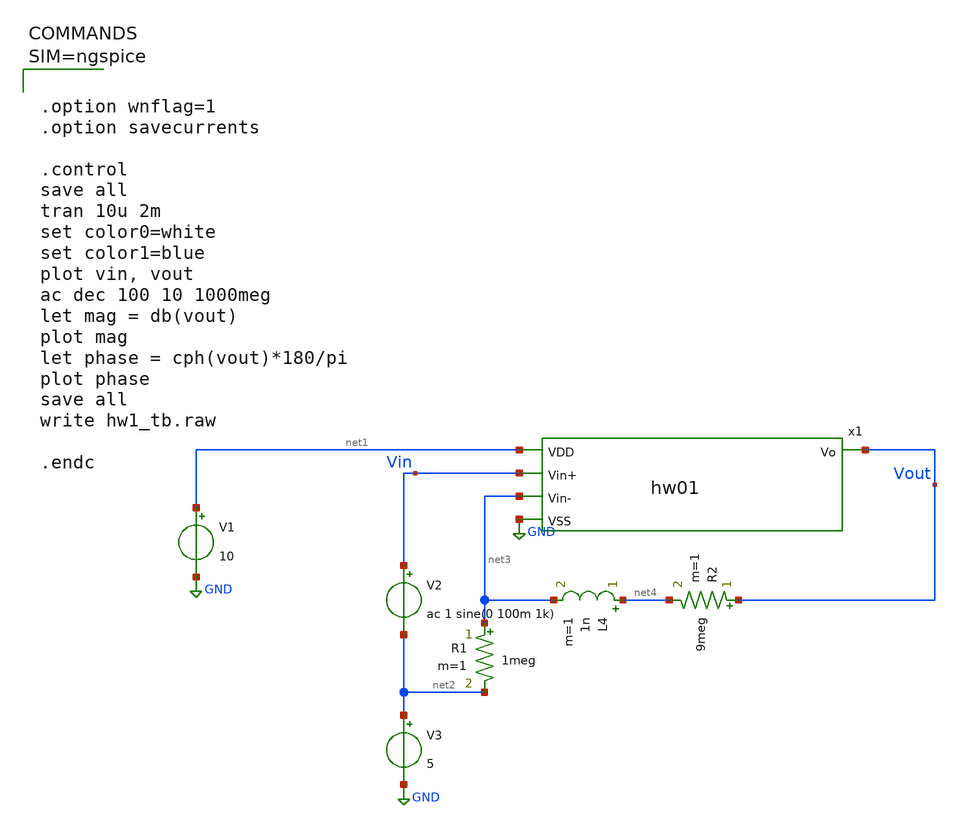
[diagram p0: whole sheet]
** sch_path: hw01/xschem/untitled.sch
**.subckt untitled
x1 net1 Vin net3 Vout GND hw01
V1 net1 GND 10
V2 Vin net2 ac 1 sine(0 100m 1k)
V3 net2 GND 5
R1 net3 net2 1meg m=1
R2 Vout net4 9meg m=1
L4 net4 net3 1n m=1
**** begin user architecture code



.option wnflag=1
.option savecurrents

.control
save all
tran 10u 2m
set color0=white
set color1=blue
plot vin, vout
ac dec 100 10 1000meg
let mag = db(vout)
plot mag
let phase = cph(vout)*180/pi
plot phase
save all
write hw1_tb.raw

.endc




** opencircuitdesign pdks install
.lib $::SKYWATER_MODELS/sky130.lib.spice tt


**** end user architecture code
**.ends

* expanding   symbol:  hw01.sym # of pins=5
** sym_path: hw01/xschem/hw01.sym
** sch_path: hw01/xschem/hw01.sch
.subckt hw01 VDD Vin+ Vin- Vo VSS
*.ipin VDD
*.ipin Vin-
*.ipin Vin+
*.ipin VSS
*.opin Vo
XM4 net4 Vin+ net2 VSS sky130_fd_pr__nfet_g5v0d10v5 L=.5 W=20 nf=1 ad='int((nf+1)/2) * W/nf * 0.29' as='int((nf+2)/2) * W/nf * 0.29'
+ pd='2*int((nf+1)/2) * (W/nf + 0.29)' ps='2*int((nf+2)/2) * (W/nf + 0.29)' nrd='0.29 / W' nrs='0.29 / W'
+ sa=0 sb=0 sd=0 mult=1 m=1
XM5 net3 net3 VSS VSS sky130_fd_pr__nfet_g5v0d10v5 L=.5 W=5 nf=1 ad='int((nf+1)/2) * W/nf * 0.29' as='int((nf+2)/2) * W/nf * 0.29'
+ pd='2*int((nf+1)/2) * (W/nf + 0.29)' ps='2*int((nf+2)/2) * (W/nf + 0.29)' nrd='0.29 / W' nrs='0.29 / W'
+ sa=0 sb=0 sd=0 mult=1 m=1
XM6 net2 net3 VSS VSS sky130_fd_pr__nfet_g5v0d10v5 L=.5 W=5 nf=1 ad='int((nf+1)/2) * W/nf * 0.29' as='int((nf+2)/2) * W/nf * 0.29'
+ pd='2*int((nf+1)/2) * (W/nf + 0.29)' ps='2*int((nf+2)/2) * (W/nf + 0.29)' nrd='0.29 / W' nrs='0.29 / W'
+ sa=0 sb=0 sd=0 mult=1 m=1
XM8 Vo net3 VSS VSS sky130_fd_pr__nfet_g5v0d10v5 L=1 W=15 nf=1 ad='int((nf+1)/2) * W/nf * 0.29' as='int((nf+2)/2) * W/nf * 0.29'
+ pd='2*int((nf+1)/2) * (W/nf + 0.29)' ps='2*int((nf+2)/2) * (W/nf + 0.29)' nrd='0.29 / W' nrs='0.29 / W'
+ sa=0 sb=0 sd=0 mult=1 m=1
XM7 net1 Vin- net2 VSS sky130_fd_pr__nfet_g5v0d10v5 L=.5 W=20 nf=1 ad='int((nf+1)/2) * W/nf * 0.29' as='int((nf+2)/2) * W/nf * 0.29'
+ pd='2*int((nf+1)/2) * (W/nf + 0.29)' ps='2*int((nf+2)/2) * (W/nf + 0.29)' nrd='0.29 / W' nrs='0.29 / W'
+ sa=0 sb=0 sd=0 mult=1 m=1
Current_source net3 net3 0
.save i(current_source)
XC1 Vo net4 sky130_fd_pr__cap_mim_m3_1 W=30 L=30 MF=1 m=1
XR2 net3 VDD VDD sky130_fd_pr__res_xhigh_po_0p69 L=0.69*20 mult=1 m=1
XM9 Vo net4 VDD VDD sky130_fd_pr__pfet_g5v0d10v5 L=.7 W=10 nf=1 ad='int((nf+1)/2) * W/nf * 0.29' as='int((nf+2)/2) * W/nf * 0.29'
+ pd='2*int((nf+1)/2) * (W/nf + 0.29)' ps='2*int((nf+2)/2) * (W/nf + 0.29)' nrd='0.29 / W' nrs='0.29 / W'
+ sa=0 sb=0 sd=0 mult=1 m=1
XM2 net4 net1 VDD VDD sky130_fd_pr__pfet_g5v0d10v5 L=1 W=10 nf=1 ad='int((nf+1)/2) * W/nf * 0.29' as='int((nf+2)/2) * W/nf * 0.29'
+ pd='2*int((nf+1)/2) * (W/nf + 0.29)' ps='2*int((nf+2)/2) * (W/nf + 0.29)' nrd='0.29 / W' nrs='0.29 / W'
+ sa=0 sb=0 sd=0 mult=1 m=1
XM1 net1 net1 VDD VDD sky130_fd_pr__pfet_g5v0d10v5 L=1 W=10 nf=1 ad='int((nf+1)/2) * W/nf * 0.29' as='int((nf+2)/2) * W/nf * 0.29'
+ pd='2*int((nf+1)/2) * (W/nf + 0.29)' ps='2*int((nf+2)/2) * (W/nf + 0.29)' nrd='0.29 / W' nrs='0.29 / W'
+ sa=0 sb=0 sd=0 mult=1 m=1
XC2 Vo net4 sky130_fd_pr__cap_mim_m3_1 W=30 L=30 MF=1 m=1
XC3 Vo net4 sky130_fd_pr__cap_mim_m3_1 W=30 L=30 MF=1 m=1
XC4 Vo net4 sky130_fd_pr__cap_mim_m3_1 W=30 L=30 MF=1 m=1
.ends

.GLOBAL GND
.end
